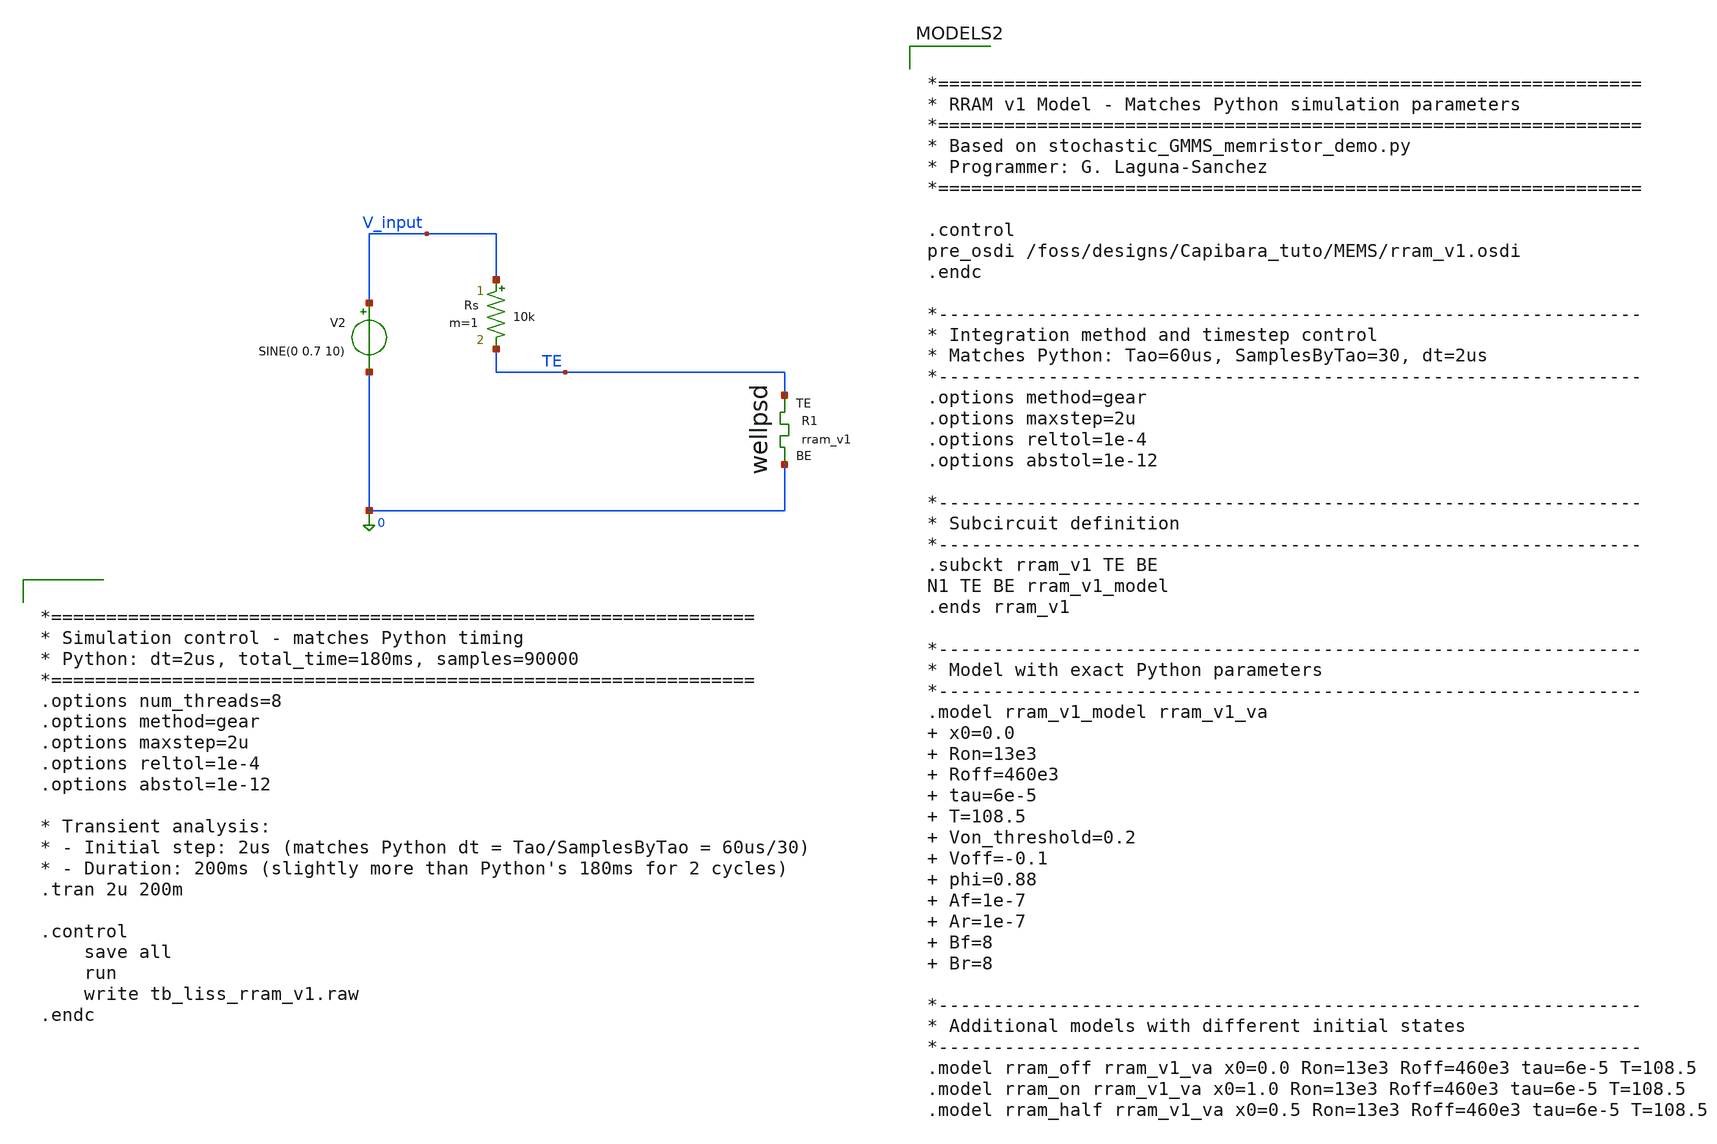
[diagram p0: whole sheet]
** sch_path: tb_liss_rram_v1_with_Rs.sch
**.subckt tb_liss_rram_v1_with_Rs
V2 V_input 0 SINE(0 0.7 10)
XR1 TE 0 rram_v1
Rs V_input TE 10k m=1
**** begin user architecture code


*================================================================
* Simulation control - matches Python timing
* Python: dt=2us, total_time=180ms, samples=90000
*================================================================
.options num_threads=8
.options method=gear
.options maxstep=2u
.options reltol=1e-4
.options abstol=1e-12

* Transient analysis:
* - Initial step: 2us (matches Python dt = Tao/SamplesByTao = 60us/30)
* - Duration: 200ms (slightly more than Python's 180ms for 2 cycles)
.tran 2u 200m

.control
	save all
	run
	write tb_liss_rram_v1.raw
.endc



*================================================================
* RRAM v1 Model - Matches Python simulation parameters
*================================================================
* Based on stochastic_GMMS_memristor_demo.py
* Programmer: G. Laguna-Sanchez
*================================================================

.control
pre_osdi /foss/designs/Capibara_tuto/MEMS/rram_v1.osdi
.endc

*----------------------------------------------------------------
* Integration method and timestep control
* Matches Python: Tao=60us, SamplesByTao=30, dt=2us
*----------------------------------------------------------------
.options method=gear
.options maxstep=2u
.options reltol=1e-4
.options abstol=1e-12

*----------------------------------------------------------------
* Subcircuit definition
*----------------------------------------------------------------
.subckt rram_v1 TE BE
N1 TE BE rram_v1_model
.ends rram_v1

*----------------------------------------------------------------
* Model with exact Python parameters
*----------------------------------------------------------------
.model rram_v1_model rram_v1_va   x0=0.0  Ron=13e3  Roff=460e3  tau=6e-5  T=108.5  Von_threshold=0.2  Voff=-0.1  phi=0.88  Af=1e-7  Ar=1e-7  Bf=8  Br=8

*----------------------------------------------------------------
* Additional models with different initial states
*----------------------------------------------------------------
.model rram_off rram_v1_va x0=0.0 Ron=13e3 Roff=460e3 tau=6e-5 T=108.5
.model rram_on rram_v1_va x0=1.0 Ron=13e3 Roff=460e3 tau=6e-5 T=108.5
.model rram_half rram_v1_va x0=0.5 Ron=13e3 Roff=460e3 tau=6e-5 T=108.5

**** end user architecture code
**.ends
.end
